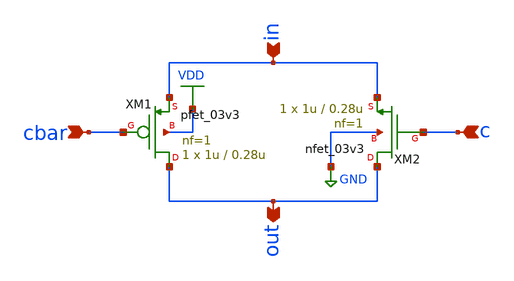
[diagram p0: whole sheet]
** sch_path: TGATE/TGATE.sch
**.subckt TGATE in out cbar c
*.ipin in
*.opin out
*.ipin cbar
*.ipin c
XM1 out cbar in VDD pfet_03v3 L=0.28u W=1u nf=1 ad='int((nf+1)/2) * W/nf * 0.18u' as='int((nf+2)/2) * W/nf * 0.18u'
+ pd='2*int((nf+1)/2) * (W/nf + 0.18u)' ps='2*int((nf+2)/2) * (W/nf + 0.18u)' nrd='0.18u / W' nrs='0.18u / W'
+ sa=0 sb=0 sd=0 m=1
XM2 out c in GND nfet_03v3 L=0.28u W=1u nf=1 ad='int((nf+1)/2) * W/nf * 0.18u' as='int((nf+2)/2) * W/nf * 0.18u'
+ pd='2*int((nf+1)/2) * (W/nf + 0.18u)' ps='2*int((nf+2)/2) * (W/nf + 0.18u)' nrd='0.18u / W' nrs='0.18u / W'
+ sa=0 sb=0 sd=0 m=1
**.ends
.GLOBAL VDD
.GLOBAL GND
.end
